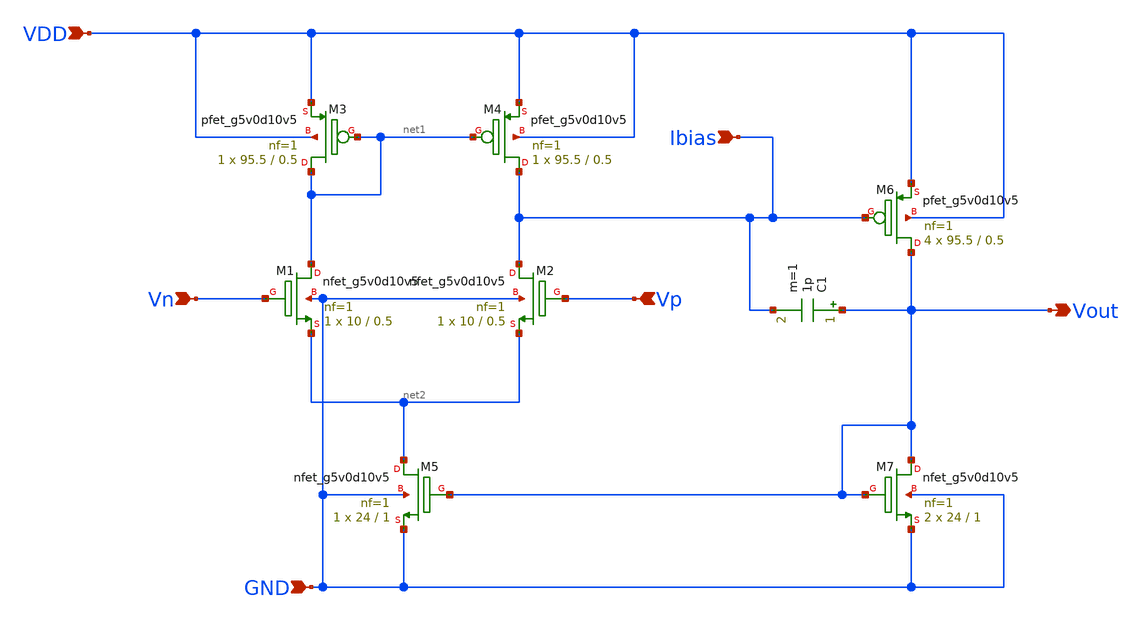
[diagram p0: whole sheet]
** sch_path: Analog_Blocks/Bandgap/Schematics/BGR_2/Miller_OTA.sch
**.subckt Miller_OTA VDD Ibias Vn Vp Vout GND
*.ipin VDD
*.ipin Ibias
*.ipin Vn
*.ipin Vp
*.opin Vout
*.ipin GND
C1 Vout Ibias 1p m=1
XM1 net1 Vn net2 GND sky130_fd_pr__nfet_g5v0d10v5 L=0.5 W=10 nf=1 ad='int((nf+1)/2) * W/nf * 0.29' as='int((nf+2)/2) * W/nf * 0.29'
+ pd='2*int((nf+1)/2) * (W/nf + 0.29)' ps='2*int((nf+2)/2) * (W/nf + 0.29)' nrd='0.29 / W' nrs='0.29 / W'
+ sa=0 sb=0 sd=0 mult=1 m=1
XM2 Ibias Vp net2 GND sky130_fd_pr__nfet_g5v0d10v5 L=0.5 W=10 nf=1 ad='int((nf+1)/2) * W/nf * 0.29' as='int((nf+2)/2) * W/nf * 0.29'
+ pd='2*int((nf+1)/2) * (W/nf + 0.29)' ps='2*int((nf+2)/2) * (W/nf + 0.29)' nrd='0.29 / W' nrs='0.29 / W'
+ sa=0 sb=0 sd=0 mult=1 m=1
XM3 net1 net1 VDD VDD sky130_fd_pr__pfet_g5v0d10v5 L=0.5 W=95.5 nf=1 ad='int((nf+1)/2) * W/nf * 0.29'
+ as='int((nf+2)/2) * W/nf * 0.29' pd='2*int((nf+1)/2) * (W/nf + 0.29)' ps='2*int((nf+2)/2) * (W/nf + 0.29)'
+ nrd='0.29 / W' nrs='0.29 / W' sa=0 sb=0 sd=0 mult=1 m=1
XM4 Ibias net1 VDD VDD sky130_fd_pr__pfet_g5v0d10v5 L=0.5 W=95.5 nf=1 ad='int((nf+1)/2) * W/nf * 0.29'
+ as='int((nf+2)/2) * W/nf * 0.29' pd='2*int((nf+1)/2) * (W/nf + 0.29)' ps='2*int((nf+2)/2) * (W/nf + 0.29)'
+ nrd='0.29 / W' nrs='0.29 / W' sa=0 sb=0 sd=0 mult=1 m=1
XM6 Vout Ibias VDD VDD sky130_fd_pr__pfet_g5v0d10v5 L=0.5 W=95.5 nf=1 ad='int((nf+1)/2) * W/nf * 0.29'
+ as='int((nf+2)/2) * W/nf * 0.29' pd='2*int((nf+1)/2) * (W/nf + 0.29)' ps='2*int((nf+2)/2) * (W/nf + 0.29)'
+ nrd='0.29 / W' nrs='0.29 / W' sa=0 sb=0 sd=0 mult=4 m=4
XM5 net2 Vout GND GND sky130_fd_pr__nfet_g5v0d10v5 L=1 W=24 nf=1 ad='int((nf+1)/2) * W/nf * 0.29' as='int((nf+2)/2) * W/nf * 0.29'
+ pd='2*int((nf+1)/2) * (W/nf + 0.29)' ps='2*int((nf+2)/2) * (W/nf + 0.29)' nrd='0.29 / W' nrs='0.29 / W'
+ sa=0 sb=0 sd=0 mult=1 m=1
XM7 Vout Vout GND GND sky130_fd_pr__nfet_g5v0d10v5 L=1 W=24 nf=1 ad='int((nf+1)/2) * W/nf * 0.29' as='int((nf+2)/2) * W/nf * 0.29'
+ pd='2*int((nf+1)/2) * (W/nf + 0.29)' ps='2*int((nf+2)/2) * (W/nf + 0.29)' nrd='0.29 / W' nrs='0.29 / W'
+ sa=0 sb=0 sd=0 mult=2 m=2
**.ends
.end
